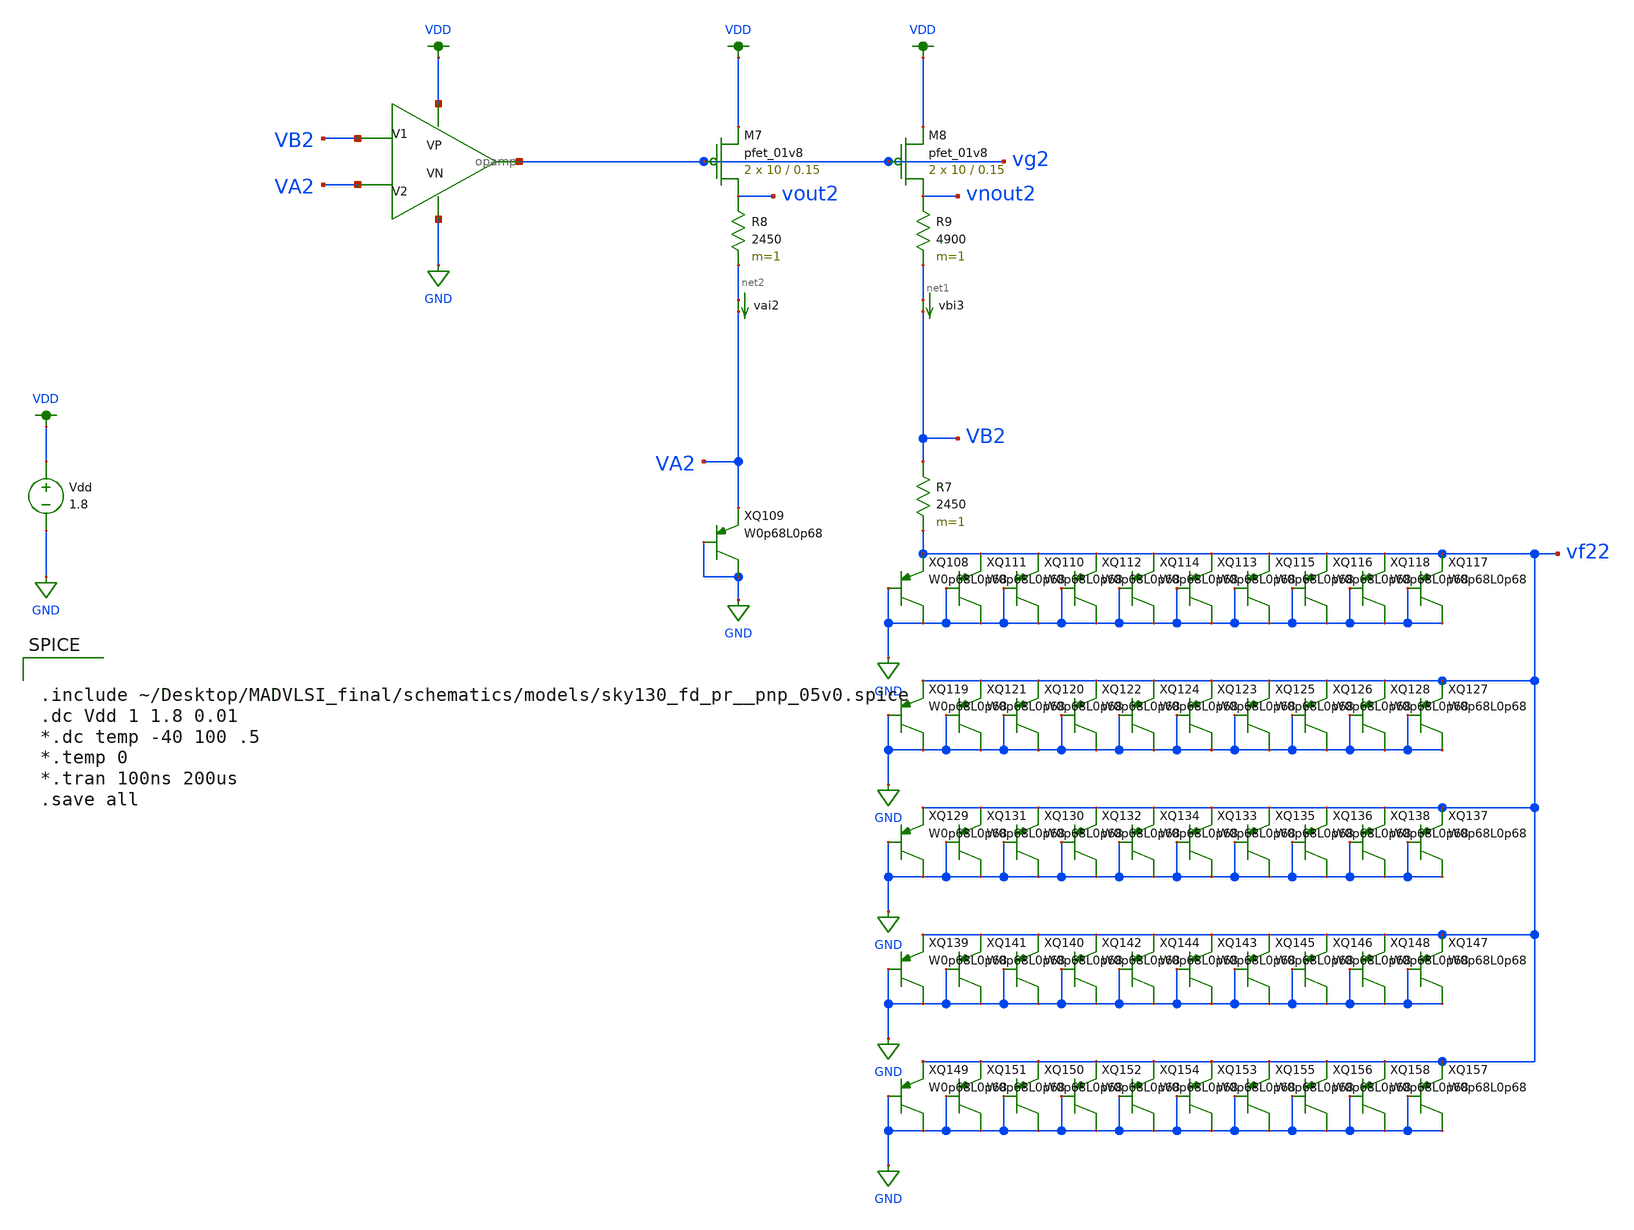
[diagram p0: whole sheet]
** sch_path: schematics/bandgap_1.sch
**.subckt bandgap_1
Vdd VDD GND 1.8
XM7 vout2 vg2 VDD VDD sky130_fd_pr__pfet_01v8 L=0.15 W=10 nf=1 ad='int((nf+1)/2) * W/nf * 0.29' as='int((nf+2)/2) * W/nf * 0.29'
+ pd='2*int((nf+1)/2) * (W/nf + 0.29)' ps='2*int((nf+2)/2) * (W/nf + 0.29)' nrd='0.29 / W' nrs='0.29 / W'
+ sa=0 sb=0 sd=0 mult=2 m=2
XQ108 vf22 GND GND sky130_fd_pr__pnp_05v0
XQ109 VA2 GND GND sky130_fd_pr__pnp_05v0
R7 VB2 vf22 2450 m=1
XQ110 vf22 GND GND sky130_fd_pr__pnp_05v0
XQ111 vf22 GND GND sky130_fd_pr__pnp_05v0
XQ112 vf22 GND GND sky130_fd_pr__pnp_05v0
XQ113 vf22 GND GND sky130_fd_pr__pnp_05v0
XQ114 vf22 GND GND sky130_fd_pr__pnp_05v0
XQ115 vf22 GND GND sky130_fd_pr__pnp_05v0
XQ116 vf22 GND GND sky130_fd_pr__pnp_05v0
XQ117 vf22 GND GND sky130_fd_pr__pnp_05v0
XQ118 vf22 GND GND sky130_fd_pr__pnp_05v0
XQ119 vf22 GND GND sky130_fd_pr__pnp_05v0
XQ120 vf22 GND GND sky130_fd_pr__pnp_05v0
XQ121 vf22 GND GND sky130_fd_pr__pnp_05v0
XQ122 vf22 GND GND sky130_fd_pr__pnp_05v0
XQ123 vf22 GND GND sky130_fd_pr__pnp_05v0
XQ124 vf22 GND GND sky130_fd_pr__pnp_05v0
XQ125 vf22 GND GND sky130_fd_pr__pnp_05v0
XQ126 vf22 GND GND sky130_fd_pr__pnp_05v0
XQ127 vf22 GND GND sky130_fd_pr__pnp_05v0
XQ128 vf22 GND GND sky130_fd_pr__pnp_05v0
XQ129 vf22 GND GND sky130_fd_pr__pnp_05v0
XQ130 vf22 GND GND sky130_fd_pr__pnp_05v0
XQ131 vf22 GND GND sky130_fd_pr__pnp_05v0
XQ132 vf22 GND GND sky130_fd_pr__pnp_05v0
XQ133 vf22 GND GND sky130_fd_pr__pnp_05v0
XQ134 vf22 GND GND sky130_fd_pr__pnp_05v0
XQ135 vf22 GND GND sky130_fd_pr__pnp_05v0
XQ136 vf22 GND GND sky130_fd_pr__pnp_05v0
XQ137 vf22 GND GND sky130_fd_pr__pnp_05v0
XQ138 vf22 GND GND sky130_fd_pr__pnp_05v0
XQ139 vf22 GND GND sky130_fd_pr__pnp_05v0
XQ140 vf22 GND GND sky130_fd_pr__pnp_05v0
XQ141 vf22 GND GND sky130_fd_pr__pnp_05v0
XQ142 vf22 GND GND sky130_fd_pr__pnp_05v0
XQ143 vf22 GND GND sky130_fd_pr__pnp_05v0
XQ144 vf22 GND GND sky130_fd_pr__pnp_05v0
XQ145 vf22 GND GND sky130_fd_pr__pnp_05v0
XQ146 vf22 GND GND sky130_fd_pr__pnp_05v0
XQ147 vf22 GND GND sky130_fd_pr__pnp_05v0
XQ148 vf22 GND GND sky130_fd_pr__pnp_05v0
XQ149 vf22 GND GND sky130_fd_pr__pnp_05v0
XQ150 vf22 GND GND sky130_fd_pr__pnp_05v0
XQ151 vf22 GND GND sky130_fd_pr__pnp_05v0
XQ152 vf22 GND GND sky130_fd_pr__pnp_05v0
XQ153 vf22 GND GND sky130_fd_pr__pnp_05v0
XQ154 vf22 GND GND sky130_fd_pr__pnp_05v0
XQ155 vf22 GND GND sky130_fd_pr__pnp_05v0
XQ156 vf22 GND GND sky130_fd_pr__pnp_05v0
XQ157 vf22 GND GND sky130_fd_pr__pnp_05v0
XQ158 vf22 GND GND sky130_fd_pr__pnp_05v0
vai2 net2 VA2 0
.save i(vai2)
vbi3 net1 VB2 0
.save i(vbi3)
X159 VB2 VA2 VDD GND vg2 opamp
R8 vout2 net2 2450 m=1
R9 vnout2 net1 4900 m=1
XM8 vnout2 vg2 VDD VDD sky130_fd_pr__pfet_01v8 L=0.15 W=10 nf=1 ad='int((nf+1)/2) * W/nf * 0.29' as='int((nf+2)/2) * W/nf * 0.29'
+ pd='2*int((nf+1)/2) * (W/nf + 0.29)' ps='2*int((nf+2)/2) * (W/nf + 0.29)' nrd='0.29 / W' nrs='0.29 / W'
+ sa=0 sb=0 sd=0 mult=2 m=2
**** begin user architecture code

.option wnflag=1
.param MC_SWITCH=0.0
.lib ~/skywater/skywater-pdk/libraries/sky130_fd_pr_ngspice/latest/models/sky130.lib.spice tt



.include ~/Desktop/MADVLSI_final/schematics/models/sky130_fd_pr__pnp_05v0.spice
.dc Vdd 1 1.8 0.01
*.dc temp -40 100 .5
*.temp 0
*.tran 100ns 200us
.save all


**** end user architecture code
**.ends

* expanding   symbol:  /home/madvlsi/Desktop/MADVLSI_final/schematics/opamp.sym # of pins=5
** sym_path: schematics/opamp.sym
** sch_path: schematics/opamp.sch
.subckt opamp V1 V2 VP VN Vout
*.ipin V1
*.ipin V2
*.opin Vout
*.iopin VP
*.iopin VN
*.iopin VP
*.iopin VN
XM1 VN net7 net2 GND sky130_fd_pr__nfet_01v8 L=l W=w nf=1 ad='int((nf+1)/2) * W/nf * 0.29' as='int((nf+2)/2) * W/nf * 0.29'
+ pd='2*int((nf+1)/2) * (W/nf + 0.29)' ps='2*int((nf+2)/2) * (W/nf + 0.29)' nrd='0.29 / W' nrs='0.29 / W'
+ sa=0 sb=0 sd=0 mult=1 m=1
XM2 VP net3 net1 VDD sky130_fd_pr__pfet_01v8 L=l W=w nf=1 ad='int((nf+1)/2) * W/nf * 0.29' as='int((nf+2)/2) * W/nf * 0.29'
+ pd='2*int((nf+1)/2) * (W/nf + 0.29)' ps='2*int((nf+2)/2) * (W/nf + 0.29)' nrd='0.29 / W' nrs='0.29 / W'
+ sa=0 sb=0 sd=0 mult=1 m=1
XM3 net1 V1 Vd VDD sky130_fd_pr__pfet_01v8 L=l W=w nf=1 ad='int((nf+1)/2) * W/nf * 0.29' as='int((nf+2)/2) * W/nf * 0.29'
+ pd='2*int((nf+1)/2) * (W/nf + 0.29)' ps='2*int((nf+2)/2) * (W/nf + 0.29)' nrd='0.29 / W' nrs='0.29 / W'
+ sa=0 sb=0 sd=0 mult=1 m=1
XM4 Vc V2 net1 VDD sky130_fd_pr__pfet_01v8 L=l W=w nf=1 ad='int((nf+1)/2) * W/nf * 0.29' as='int((nf+2)/2) * W/nf * 0.29'
+ pd='2*int((nf+1)/2) * (W/nf + 0.29)' ps='2*int((nf+2)/2) * (W/nf + 0.29)' nrd='0.29 / W' nrs='0.29 / W'
+ sa=0 sb=0 sd=0 mult=1 m=1
XM5 Va V2 net2 GND sky130_fd_pr__nfet_01v8 L=l W=w nf=1 ad='int((nf+1)/2) * W/nf * 0.29' as='int((nf+2)/2) * W/nf * 0.29'
+ pd='2*int((nf+1)/2) * (W/nf + 0.29)' ps='2*int((nf+2)/2) * (W/nf + 0.29)' nrd='0.29 / W' nrs='0.29 / W'
+ sa=0 sb=0 sd=0 mult=1 m=1
XM6 net2 V1 Vb GND sky130_fd_pr__nfet_01v8 L=l W=w nf=1 ad='int((nf+1)/2) * W/nf * 0.29' as='int((nf+2)/2) * W/nf * 0.29'
+ pd='2*int((nf+1)/2) * (W/nf + 0.29)' ps='2*int((nf+2)/2) * (W/nf + 0.29)' nrd='0.29 / W' nrs='0.29 / W'
+ sa=0 sb=0 sd=0 mult=1 m=1
XM7 net3 net3 Va VDD sky130_fd_pr__pfet_01v8 L=l W=w nf=1 ad='int((nf+1)/2) * W/nf * 0.29' as='int((nf+2)/2) * W/nf * 0.29'
+ pd='2*int((nf+1)/2) * (W/nf + 0.29)' ps='2*int((nf+2)/2) * (W/nf + 0.29)' nrd='0.29 / W' nrs='0.29 / W'
+ sa=0 sb=0 sd=0 mult=1 m=1
XM8 net6 net6 Va VDD sky130_fd_pr__pfet_01v8 L=l W=w nf=1 ad='int((nf+1)/2) * W/nf * 0.29' as='int((nf+2)/2) * W/nf * 0.29'
+ pd='2*int((nf+1)/2) * (W/nf + 0.29)' ps='2*int((nf+2)/2) * (W/nf + 0.29)' nrd='0.29 / W' nrs='0.29 / W'
+ sa=0 sb=0 sd=0 mult=1 m=1
XM9 net5 net6 Vb VDD sky130_fd_pr__pfet_01v8 L=l W=w nf=1 ad='int((nf+1)/2) * W/nf * 0.29' as='int((nf+2)/2) * W/nf * 0.29'
+ pd='2*int((nf+1)/2) * (W/nf + 0.29)' ps='2*int((nf+2)/2) * (W/nf + 0.29)' nrd='0.29 / W' nrs='0.29 / W'
+ sa=0 sb=0 sd=0 mult=1 m=1
XM10 Va net3 VP VDD sky130_fd_pr__pfet_01v8 L=l W=w nf=1 ad='int((nf+1)/2) * W/nf * 0.29' as='int((nf+2)/2) * W/nf * 0.29'
+ pd='2*int((nf+1)/2) * (W/nf + 0.29)' ps='2*int((nf+2)/2) * (W/nf + 0.29)' nrd='0.29 / W' nrs='0.29 / W'
+ sa=0 sb=0 sd=0 mult=1 m=1
XM11 Vb net3 VP VDD sky130_fd_pr__pfet_01v8 L=l W=w nf=1 ad='int((nf+1)/2) * W/nf * 0.29' as='int((nf+2)/2) * W/nf * 0.29'
+ pd='2*int((nf+1)/2) * (W/nf + 0.29)' ps='2*int((nf+2)/2) * (W/nf + 0.29)' nrd='0.29 / W' nrs='0.29 / W'
+ sa=0 sb=0 sd=0 mult=1 m=1
XM12 net6 net6 Vc GND sky130_fd_pr__nfet_01v8 L=l W=w nf=1 ad='int((nf+1)/2) * W/nf * 0.29' as='int((nf+2)/2) * W/nf * 0.29'
+ pd='2*int((nf+1)/2) * (W/nf + 0.29)' ps='2*int((nf+2)/2) * (W/nf + 0.29)' nrd='0.29 / W' nrs='0.29 / W'
+ sa=0 sb=0 sd=0 mult=1 m=1
XM13 net5 net6 Vd GND sky130_fd_pr__nfet_01v8 L=l W=w nf=1 ad='int((nf+1)/2) * W/nf * 0.29' as='int((nf+2)/2) * W/nf * 0.29'
+ pd='2*int((nf+1)/2) * (W/nf + 0.29)' ps='2*int((nf+2)/2) * (W/nf + 0.29)' nrd='0.29 / W' nrs='0.29 / W'
+ sa=0 sb=0 sd=0 mult=1 m=1
XM14 Vc net7 VN GND sky130_fd_pr__nfet_01v8 L=l W=w nf=1 ad='int((nf+1)/2) * W/nf * 0.29' as='int((nf+2)/2) * W/nf * 0.29'
+ pd='2*int((nf+1)/2) * (W/nf + 0.29)' ps='2*int((nf+2)/2) * (W/nf + 0.29)' nrd='0.29 / W' nrs='0.29 / W'
+ sa=0 sb=0 sd=0 mult=1 m=1
XM15 Vd net7 VN GND sky130_fd_pr__nfet_01v8 L=l W=w nf=1 ad='int((nf+1)/2) * W/nf * 0.29' as='int((nf+2)/2) * W/nf * 0.29'
+ pd='2*int((nf+1)/2) * (W/nf + 0.29)' ps='2*int((nf+2)/2) * (W/nf + 0.29)' nrd='0.29 / W' nrs='0.29 / W'
+ sa=0 sb=0 sd=0 mult=1 m=1
XM16 net8 net7 net3 GND sky130_fd_pr__nfet_01v8 L=l W=w nf=1 ad='int((nf+1)/2) * W/nf * 0.29' as='int((nf+2)/2) * W/nf * 0.29'
+ pd='2*int((nf+1)/2) * (W/nf + 0.29)' ps='2*int((nf+2)/2) * (W/nf + 0.29)' nrd='0.29 / W' nrs='0.29 / W'
+ sa=0 sb=0 sd=0 mult=1 m=1
XM17 VN net7 net8 GND sky130_fd_pr__nfet_01v8 L=l W=w nf=1 ad='int((nf+1)/2) * W/nf * 0.29' as='int((nf+2)/2) * W/nf * 0.29'
+ pd='2*int((nf+1)/2) * (W/nf + 0.29)' ps='2*int((nf+2)/2) * (W/nf + 0.29)' nrd='0.29 / W' nrs='0.29 / W'
+ sa=0 sb=0 sd=0 mult=1 m=1
XM18 net8 net7 VP GND sky130_fd_pr__nfet_01v8 L=l W=w nf=1 ad='int((nf+1)/2) * W/nf * 0.29' as='int((nf+2)/2) * W/nf * 0.29'
+ pd='2*int((nf+1)/2) * (W/nf + 0.29)' ps='2*int((nf+2)/2) * (W/nf + 0.29)' nrd='0.29 / W' nrs='0.29 / W'
+ sa=0 sb=0 sd=0 mult=M m=M
XM19 net4 net3 net7 VDD sky130_fd_pr__pfet_01v8 L=l W=w nf=1 ad='int((nf+1)/2) * W/nf * 0.29' as='int((nf+2)/2) * W/nf * 0.29'
+ pd='2*int((nf+1)/2) * (W/nf + 0.29)' ps='2*int((nf+2)/2) * (W/nf + 0.29)' nrd='0.29 / W' nrs='0.29 / W'
+ sa=0 sb=0 sd=0 mult=1 m=1
XM20 VP net3 net4 VDD sky130_fd_pr__pfet_01v8 L=l W=w nf=1 ad='int((nf+1)/2) * W/nf * 0.29' as='int((nf+2)/2) * W/nf * 0.29'
+ pd='2*int((nf+1)/2) * (W/nf + 0.29)' ps='2*int((nf+2)/2) * (W/nf + 0.29)' nrd='0.29 / W' nrs='0.29 / W'
+ sa=0 sb=0 sd=0 mult=1 m=1
XM21 net4 net3 VN VDD sky130_fd_pr__pfet_01v8 L=l W=w nf=1 ad='int((nf+1)/2) * W/nf * 0.29' as='int((nf+2)/2) * W/nf * 0.29'
+ pd='2*int((nf+1)/2) * (W/nf + 0.29)' ps='2*int((nf+2)/2) * (W/nf + 0.29)' nrd='0.29 / W' nrs='0.29 / W'
+ sa=0 sb=0 sd=0 mult=M m=M
XM22 net7 net7 Vc GND sky130_fd_pr__nfet_01v8 L=l W=w nf=1 ad='int((nf+1)/2) * W/nf * 0.29' as='int((nf+2)/2) * W/nf * 0.29'
+ pd='2*int((nf+1)/2) * (W/nf + 0.29)' ps='2*int((nf+2)/2) * (W/nf + 0.29)' nrd='0.29 / W' nrs='0.29 / W'
+ sa=0 sb=0 sd=0 mult=1 m=1
**** begin user architecture code

.param M=3
.param w=3
.param l=0.6


**** end user architecture code
XM23 Vout net5 VN GND sky130_fd_pr__nfet_01v8 L=.15 W=6 nf=1 ad='int((nf+1)/2) * W/nf * 0.29' as='int((nf+2)/2) * W/nf * 0.29'
+ pd='2*int((nf+1)/2) * (W/nf + 0.29)' ps='2*int((nf+2)/2) * (W/nf + 0.29)' nrd='0.29 / W' nrs='0.29 / W'
+ sa=0 sb=0 sd=0 mult=1 m=1
XM24 Vout net5 VP VDD sky130_fd_pr__pfet_01v8 L=.15 W=12 nf=1 ad='int((nf+1)/2) * W/nf * 0.29' as='int((nf+2)/2) * W/nf * 0.29'
+ pd='2*int((nf+1)/2) * (W/nf + 0.29)' ps='2*int((nf+2)/2) * (W/nf + 0.29)' nrd='0.29 / W' nrs='0.29 / W'
+ sa=0 sb=0 sd=0 mult=1 m=1
C1 Vout net5 500f m=1
.ends

.GLOBAL VDD
.GLOBAL GND
.end
